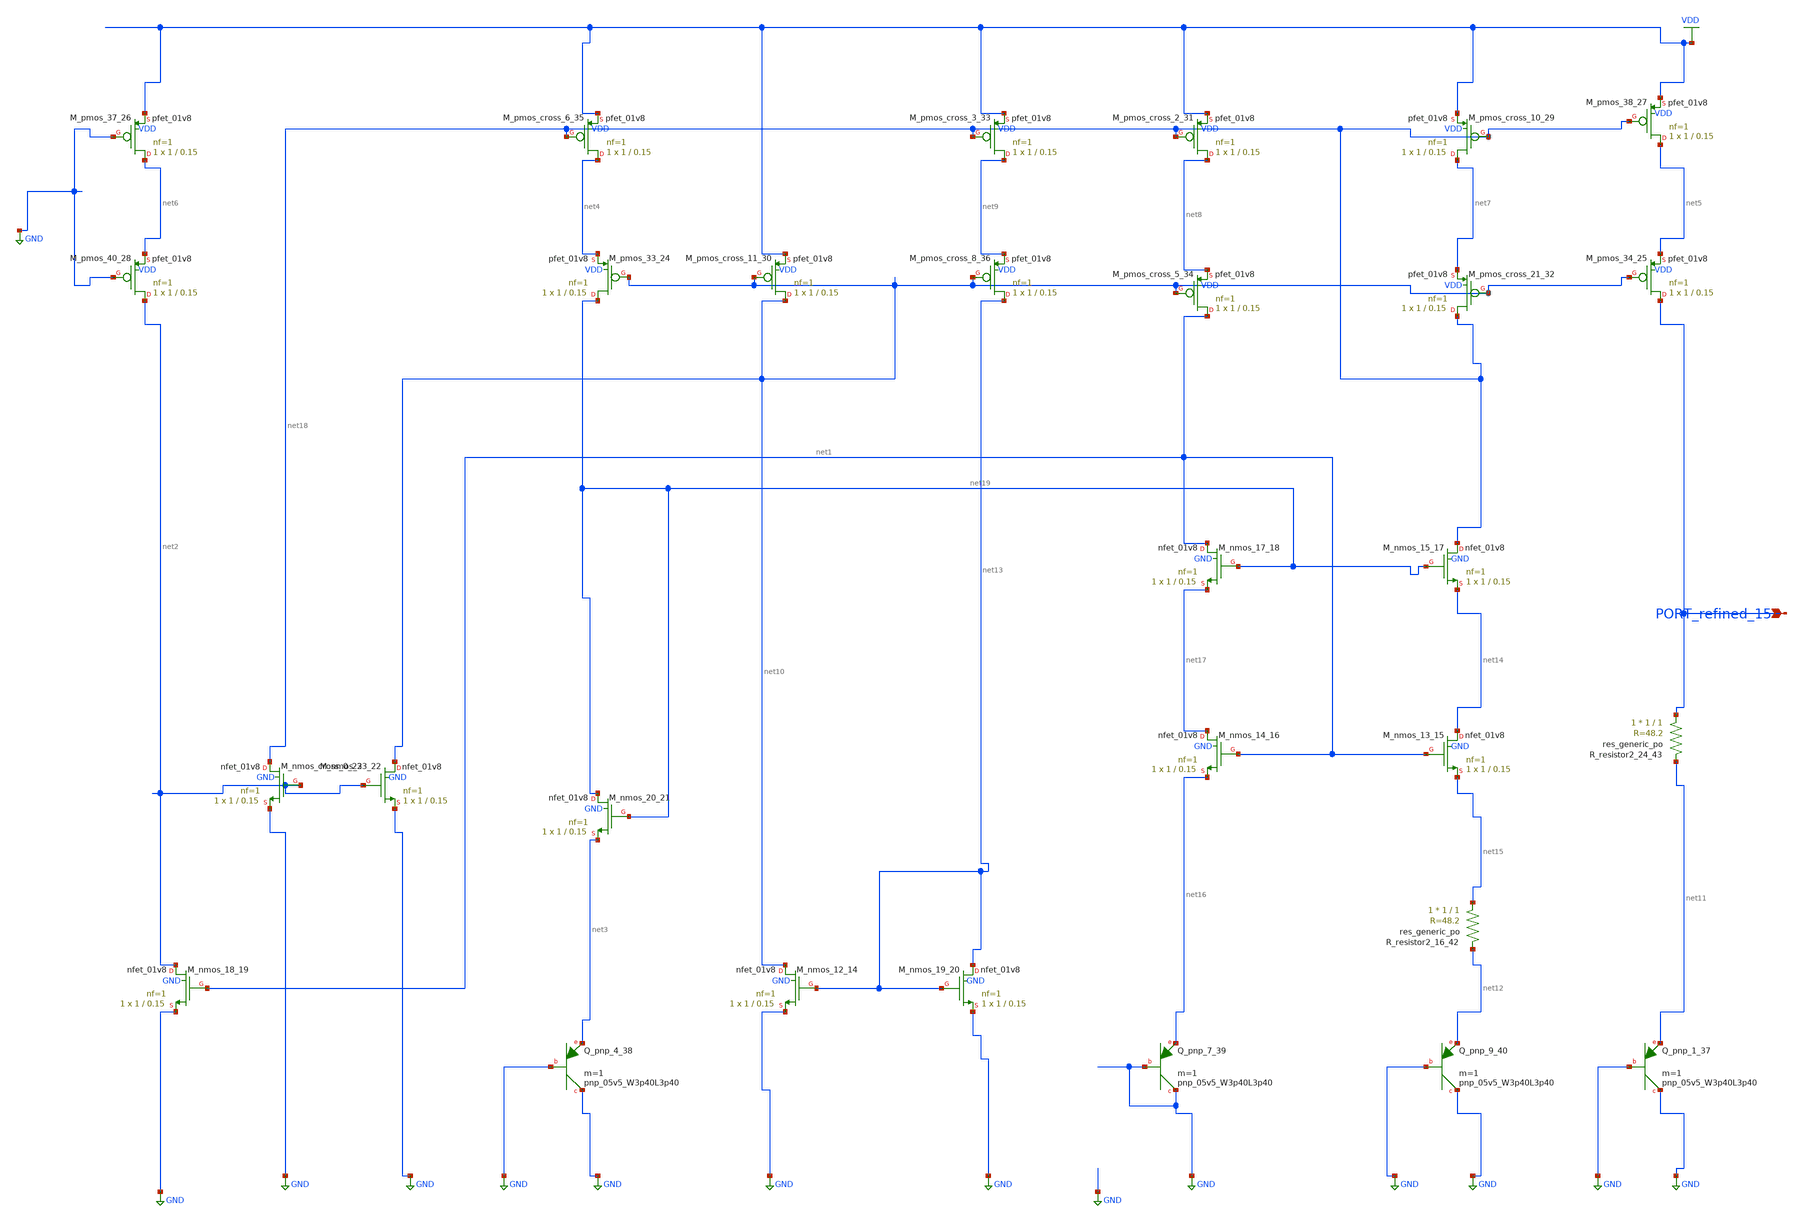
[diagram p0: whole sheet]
** sch_path: schematics/Image2Net/029.sch
**.subckt 029 PORT_refined_15
*.ipin PORT_refined_15
XM_nmos_12_14 net10 net13 GND GND sky130_fd_pr__nfet_01v8 L=0.15 W=1 nf=1 ad='int((1 + 1)/2) * 1 / 1 * 0.29'
+ as='int((1 + 2)/2) * 1 / 1 * 0.29' pd='2*int((1 + 1)/2) * (1 / 1 + 0.29)' ps='2*int((1 + 2)/2) * (1 / 1 + 0.29)'
+ nrd='0.29 / 1 ' nrs='0.29 / 1 ' sa=0 sb=0 sd=0 mult=1 m=1
XM_nmos_13_15 net14 net1 net15 GND sky130_fd_pr__nfet_01v8 L=0.15 W=1 nf=1 ad='int((1 + 1)/2) * 1 / 1 * 0.29'
+ as='int((1 + 2)/2) * 1 / 1 * 0.29' pd='2*int((1 + 1)/2) * (1 / 1 + 0.29)' ps='2*int((1 + 2)/2) * (1 / 1 + 0.29)'
+ nrd='0.29 / 1 ' nrs='0.29 / 1 ' sa=0 sb=0 sd=0 mult=1 m=1
XM_nmos_14_16 net17 net1 net16 GND sky130_fd_pr__nfet_01v8 L=0.15 W=1 nf=1 ad='int((1 + 1)/2) * 1 / 1 * 0.29'
+ as='int((1 + 2)/2) * 1 / 1 * 0.29' pd='2*int((1 + 1)/2) * (1 / 1 + 0.29)' ps='2*int((1 + 2)/2) * (1 / 1 + 0.29)'
+ nrd='0.29 / 1 ' nrs='0.29 / 1 ' sa=0 sb=0 sd=0 mult=1 m=1
XM_nmos_15_17 net18 net19 net14 GND sky130_fd_pr__nfet_01v8 L=0.15 W=1 nf=1 ad='int((1 + 1)/2) * 1 / 1 * 0.29'
+ as='int((1 + 2)/2) * 1 / 1 * 0.29' pd='2*int((1 + 1)/2) * (1 / 1 + 0.29)' ps='2*int((1 + 2)/2) * (1 / 1 + 0.29)'
+ nrd='0.29 / 1 ' nrs='0.29 / 1 ' sa=0 sb=0 sd=0 mult=1 m=1
XM_nmos_17_18 net1 net19 net17 GND sky130_fd_pr__nfet_01v8 L=0.15 W=1 nf=1 ad='int((1 + 1)/2) * 1 / 1 * 0.29'
+ as='int((1 + 2)/2) * 1 / 1 * 0.29' pd='2*int((1 + 1)/2) * (1 / 1 + 0.29)' ps='2*int((1 + 2)/2) * (1 / 1 + 0.29)'
+ nrd='0.29 / 1 ' nrs='0.29 / 1 ' sa=0 sb=0 sd=0 mult=1 m=1
XM_nmos_18_19 net2 net1 GND GND sky130_fd_pr__nfet_01v8 L=0.15 W=1 nf=1 ad='int((1 + 1)/2) * 1 / 1 * 0.29'
+ as='int((1 + 2)/2) * 1 / 1 * 0.29' pd='2*int((1 + 1)/2) * (1 / 1 + 0.29)' ps='2*int((1 + 2)/2) * (1 / 1 + 0.29)'
+ nrd='0.29 / 1 ' nrs='0.29 / 1 ' sa=0 sb=0 sd=0 mult=1 m=1
XM_nmos_19_20 net13 net13 GND GND sky130_fd_pr__nfet_01v8 L=0.15 W=1 nf=1 ad='int((1 + 1)/2) * 1 / 1 * 0.29'
+ as='int((1 + 2)/2) * 1 / 1 * 0.29' pd='2*int((1 + 1)/2) * (1 / 1 + 0.29)' ps='2*int((1 + 2)/2) * (1 / 1 + 0.29)'
+ nrd='0.29 / 1 ' nrs='0.29 / 1 ' sa=0 sb=0 sd=0 mult=1 m=1
XM_nmos_20_21 net19 net19 net3 GND sky130_fd_pr__nfet_01v8 L=0.15 W=1 nf=1 ad='int((1 + 1)/2) * 1 / 1 * 0.29'
+ as='int((1 + 2)/2) * 1 / 1 * 0.29' pd='2*int((1 + 1)/2) * (1 / 1 + 0.29)' ps='2*int((1 + 2)/2) * (1 / 1 + 0.29)'
+ nrd='0.29 / 1 ' nrs='0.29 / 1 ' sa=0 sb=0 sd=0 mult=1 m=1
XM_nmos_23_22 net10 net2 GND GND sky130_fd_pr__nfet_01v8 L=0.15 W=1 nf=1 ad='int((1 + 1)/2) * 1 / 1 * 0.29'
+ as='int((1 + 2)/2) * 1 / 1 * 0.29' pd='2*int((1 + 1)/2) * (1 / 1 + 0.29)' ps='2*int((1 + 2)/2) * (1 / 1 + 0.29)'
+ nrd='0.29 / 1 ' nrs='0.29 / 1 ' sa=0 sb=0 sd=0 mult=1 m=1
XM_nmos_cross_0_23 net18 net2 GND GND sky130_fd_pr__nfet_01v8 L=0.15 W=1 nf=1 ad='int((1 + 1)/2) * 1 / 1 * 0.29'
+ as='int((1 + 2)/2) * 1 / 1 * 0.29' pd='2*int((1 + 1)/2) * (1 / 1 + 0.29)' ps='2*int((1 + 2)/2) * (1 / 1 + 0.29)'
+ nrd='0.29 / 1 ' nrs='0.29 / 1 ' sa=0 sb=0 sd=0 mult=1 m=1
XM_pmos_33_24 net19 net10 net4 VDD sky130_fd_pr__pfet_01v8 L=0.15 W=1 nf=1 ad='int((1 + 1)/2) * 1 / 1 * 0.29'
+ as='int((1 + 2)/2) * 1 / 1 * 0.29' pd='2*int((1 + 1)/2) * (1 / 1 + 0.29)' ps='2*int((1 + 2)/2) * (1 / 1 + 0.29)'
+ nrd='0.29 / 1 ' nrs='0.29 / 1 ' sa=0 sb=0 sd=0 mult=1 m=1
XM_pmos_34_25 PORT_refined_15 net10 net5 VDD sky130_fd_pr__pfet_01v8 L=0.15 W=1 nf=1 ad='int((1 + 1)/2) * 1 / 1 * 0.29'
+ as='int((1 + 2)/2) * 1 / 1 * 0.29' pd='2*int((1 + 1)/2) * (1 / 1 + 0.29)' ps='2*int((1 + 2)/2) * (1 / 1 + 0.29)'
+ nrd='0.29 / 1 ' nrs='0.29 / 1 ' sa=0 sb=0 sd=0 mult=1 m=1
XM_pmos_37_26 net6 GND VDD VDD sky130_fd_pr__pfet_01v8 L=0.15 W=1 nf=1 ad='int((1 + 1)/2) * 1 / 1 * 0.29'
+ as='int((1 + 2)/2) * 1 / 1 * 0.29' pd='2*int((1 + 1)/2) * (1 / 1 + 0.29)' ps='2*int((1 + 2)/2) * (1 / 1 + 0.29)'
+ nrd='0.29 / 1 ' nrs='0.29 / 1 ' sa=0 sb=0 sd=0 mult=1 m=1
XM_pmos_38_27 net5 net18 VDD VDD sky130_fd_pr__pfet_01v8 L=0.15 W=1 nf=1 ad='int((1 + 1)/2) * 1 / 1 * 0.29'
+ as='int((1 + 2)/2) * 1 / 1 * 0.29' pd='2*int((1 + 1)/2) * (1 / 1 + 0.29)' ps='2*int((1 + 2)/2) * (1 / 1 + 0.29)'
+ nrd='0.29 / 1 ' nrs='0.29 / 1 ' sa=0 sb=0 sd=0 mult=1 m=1
XM_pmos_40_28 net2 GND net6 VDD sky130_fd_pr__pfet_01v8 L=0.15 W=1 nf=1 ad='int((1 + 1)/2) * 1 / 1 * 0.29'
+ as='int((1 + 2)/2) * 1 / 1 * 0.29' pd='2*int((1 + 1)/2) * (1 / 1 + 0.29)' ps='2*int((1 + 2)/2) * (1 / 1 + 0.29)'
+ nrd='0.29 / 1 ' nrs='0.29 / 1 ' sa=0 sb=0 sd=0 mult=1 m=1
XM_pmos_cross_10_29 net7 net18 VDD VDD sky130_fd_pr__pfet_01v8 L=0.15 W=1 nf=1 ad='int((1 + 1)/2) * 1 / 1 * 0.29'
+ as='int((1 + 2)/2) * 1 / 1 * 0.29' pd='2*int((1 + 1)/2) * (1 / 1 + 0.29)' ps='2*int((1 + 2)/2) * (1 / 1 + 0.29)'
+ nrd='0.29 / 1 ' nrs='0.29 / 1 ' sa=0 sb=0 sd=0 mult=1 m=1
XM_pmos_cross_11_30 net10 net10 VDD VDD sky130_fd_pr__pfet_01v8 L=0.15 W=1 nf=1 ad='int((1 + 1)/2) * 1 / 1 * 0.29'
+ as='int((1 + 2)/2) * 1 / 1 * 0.29' pd='2*int((1 + 1)/2) * (1 / 1 + 0.29)' ps='2*int((1 + 2)/2) * (1 / 1 + 0.29)'
+ nrd='0.29 / 1 ' nrs='0.29 / 1 ' sa=0 sb=0 sd=0 mult=1 m=1
XM_pmos_cross_2_31 net8 net18 VDD VDD sky130_fd_pr__pfet_01v8 L=0.15 W=1 nf=1 ad='int((1 + 1)/2) * 1 / 1 * 0.29'
+ as='int((1 + 2)/2) * 1 / 1 * 0.29' pd='2*int((1 + 1)/2) * (1 / 1 + 0.29)' ps='2*int((1 + 2)/2) * (1 / 1 + 0.29)'
+ nrd='0.29 / 1 ' nrs='0.29 / 1 ' sa=0 sb=0 sd=0 mult=1 m=1
XM_pmos_cross_21_32 net18 net10 net7 VDD sky130_fd_pr__pfet_01v8 L=0.15 W=1 nf=1 ad='int((1 + 1)/2) * 1 / 1 * 0.29'
+ as='int((1 + 2)/2) * 1 / 1 * 0.29' pd='2*int((1 + 1)/2) * (1 / 1 + 0.29)' ps='2*int((1 + 2)/2) * (1 / 1 + 0.29)'
+ nrd='0.29 / 1 ' nrs='0.29 / 1 ' sa=0 sb=0 sd=0 mult=1 m=1
XM_pmos_cross_3_33 net9 net18 VDD VDD sky130_fd_pr__pfet_01v8 L=0.15 W=1 nf=1 ad='int((1 + 1)/2) * 1 / 1 * 0.29'
+ as='int((1 + 2)/2) * 1 / 1 * 0.29' pd='2*int((1 + 1)/2) * (1 / 1 + 0.29)' ps='2*int((1 + 2)/2) * (1 / 1 + 0.29)'
+ nrd='0.29 / 1 ' nrs='0.29 / 1 ' sa=0 sb=0 sd=0 mult=1 m=1
XM_pmos_cross_5_34 net1 net10 net8 VDD sky130_fd_pr__pfet_01v8 L=0.15 W=1 nf=1 ad='int((1 + 1)/2) * 1 / 1 * 0.29'
+ as='int((1 + 2)/2) * 1 / 1 * 0.29' pd='2*int((1 + 1)/2) * (1 / 1 + 0.29)' ps='2*int((1 + 2)/2) * (1 / 1 + 0.29)'
+ nrd='0.29 / 1 ' nrs='0.29 / 1 ' sa=0 sb=0 sd=0 mult=1 m=1
XM_pmos_cross_6_35 net4 net18 VDD VDD sky130_fd_pr__pfet_01v8 L=0.15 W=1 nf=1 ad='int((1 + 1)/2) * 1 / 1 * 0.29'
+ as='int((1 + 2)/2) * 1 / 1 * 0.29' pd='2*int((1 + 1)/2) * (1 / 1 + 0.29)' ps='2*int((1 + 2)/2) * (1 / 1 + 0.29)'
+ nrd='0.29 / 1 ' nrs='0.29 / 1 ' sa=0 sb=0 sd=0 mult=1 m=1
XM_pmos_cross_8_36 net13 net10 net9 VDD sky130_fd_pr__pfet_01v8 L=0.15 W=1 nf=1 ad='int((1 + 1)/2) * 1 / 1 * 0.29'
+ as='int((1 + 2)/2) * 1 / 1 * 0.29' pd='2*int((1 + 1)/2) * (1 / 1 + 0.29)' ps='2*int((1 + 2)/2) * (1 / 1 + 0.29)'
+ nrd='0.29 / 1 ' nrs='0.29 / 1 ' sa=0 sb=0 sd=0 mult=1 m=1
XQ_pnp_1_37 GND GND net11 sky130_fd_pr__pnp_05v5_W3p40L3p40 m=1
XQ_pnp_4_38 GND GND net3 sky130_fd_pr__pnp_05v5_W3p40L3p40 m=1
XQ_pnp_7_39 GND GND net16 sky130_fd_pr__pnp_05v5_W3p40L3p40 m=1
XQ_pnp_9_40 GND GND net12 sky130_fd_pr__pnp_05v5_W3p40L3p40 m=1
XR_resistor2_16_42 net15 net12 sky130_fd_pr__res_generic_po W=1 L=1 m=1
XR_resistor2_24_43 PORT_refined_15 net11 sky130_fd_pr__res_generic_po W=1 L=1 m=1
**.ends
.GLOBAL GND
.GLOBAL VDD
.end
